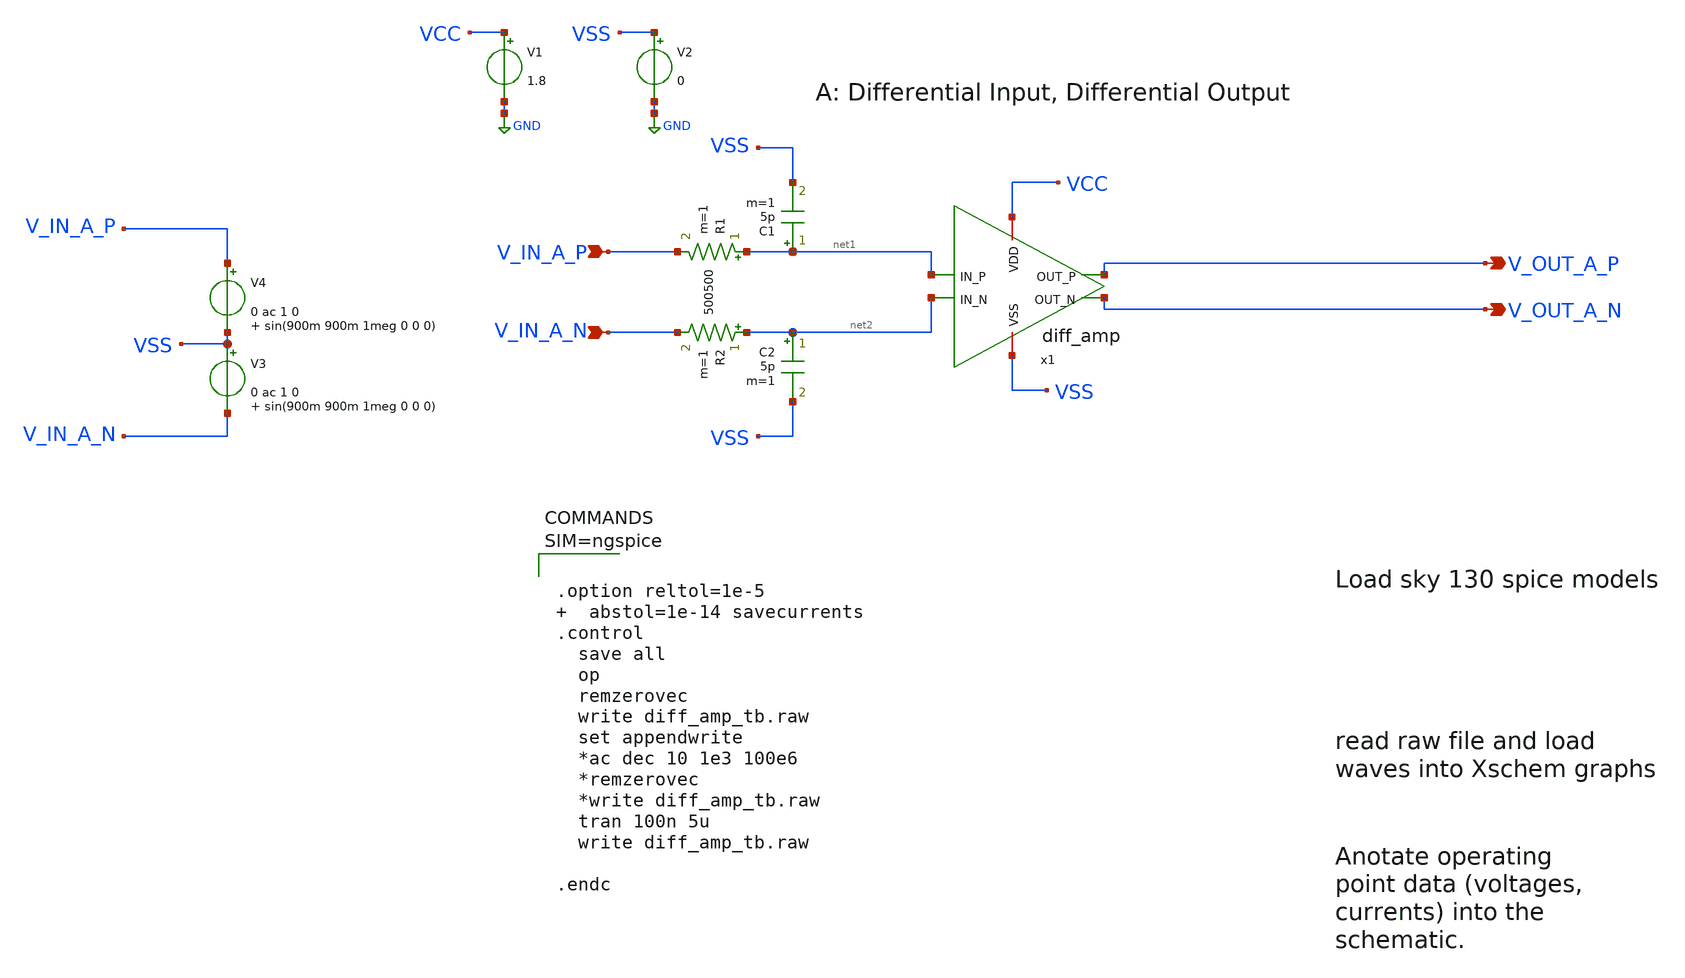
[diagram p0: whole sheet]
** sch_path: xschem/diff_amp_tb.sch
**.subckt diff_amp_tb V_IN_A_P V_OUT_A_N V_OUT_A_P V_IN_A_N
*.ipin V_IN_A_P
*.opin V_OUT_A_N
*.opin V_OUT_A_P
*.ipin V_IN_A_N
x1 VCC VSS net2 V_OUT_A_P V_OUT_A_N net1 diff_amp
V1 VCC GND 1.8
V2 VSS GND 0
V4 V_IN_A_P VSS 0 ac 1 0 sin(900m 900m 1meg 0 0 0)
R1 net1 V_IN_A_P 500 m=1
C1 net1 VSS 5p m=1
R2 net2 V_IN_A_N 500 m=1
C2 net2 VSS 5p m=1
V3 VSS V_IN_A_N 0 ac 1 0 sin(900m 900m 1meg 0 0 0)
**** begin user architecture code

** opencircuitdesign pdks install
.lib $::SKYWATER_MODELS/sky130.lib.spice tt





.option reltol=1e-5   abstol=1e-14 savecurrents
.control
  save all
  op
  remzerovec
  write diff_amp_tb.raw
  set appendwrite
  *ac dec 10 1e3 100e6
  *remzerovec
  *write diff_amp_tb.raw
  tran 100n 5u
  write diff_amp_tb.raw

.endc



**** end user architecture code
**.ends

* expanding   symbol:  diff_amp.sym # of pins=6
** sym_path: xschem/diff_amp.sym
** sch_path: xschem/diff_amp.sch
.subckt diff_amp VDD VSS IN_N OUT_P OUT_N IN_P
*.iopin VDD
*.iopin VSS
*.ipin IN_N
*.ipin IN_P
*.opin OUT_P
*.opin OUT_N
XM6 net1 net1 VSS VSS sky130_fd_pr__nfet_01v8 L=0.38 W=3.6 nf=2 ad='int((nf+1)/2) * W/nf * 0.29' as='int((nf+2)/2) * W/nf * 0.29'
+ pd='2*int((nf+1)/2) * (W/nf + 0.29)' ps='2*int((nf+2)/2) * (W/nf + 0.29)' nrd='0.29 / W' nrs='0.29 / W'
+ sa=0 sb=0 sd=0 mult=1 m=1
XM4 OUT_P OUT_P VDD VDD sky130_fd_pr__pfet_01v8_lvt L=0.38 W=3.6 nf=2 ad='int((nf+1)/2) * W/nf * 0.29'
+ as='int((nf+2)/2) * W/nf * 0.29' pd='2*int((nf+1)/2) * (W/nf + 0.29)' ps='2*int((nf+2)/2) * (W/nf + 0.29)'
+ nrd='0.29 / W' nrs='0.29 / W' sa=0 sb=0 sd=0 mult=1 m=1
XR2 net1 VDD VSS sky130_fd_pr__res_xhigh_po_2p85 L=1.85 mult=10 m=10
XM3 VX net1 VSS VSS sky130_fd_pr__nfet_01v8 L=0.38 W=3.6 nf=2 ad='int((nf+1)/2) * W/nf * 0.29' as='int((nf+2)/2) * W/nf * 0.29'
+ pd='2*int((nf+1)/2) * (W/nf + 0.29)' ps='2*int((nf+2)/2) * (W/nf + 0.29)' nrd='0.29 / W' nrs='0.29 / W'
+ sa=0 sb=0 sd=0 mult=1 m=1
XM1 OUT_P IN_P VX VSS sky130_fd_pr__nfet_01v8 L=0.38 W=3.6 nf=2 ad='int((nf+1)/2) * W/nf * 0.29' as='int((nf+2)/2) * W/nf * 0.29'
+ pd='2*int((nf+1)/2) * (W/nf + 0.29)' ps='2*int((nf+2)/2) * (W/nf + 0.29)' nrd='0.29 / W' nrs='0.29 / W'
+ sa=0 sb=0 sd=0 mult=1 m=1
XM2 OUT_N IN_N VX VSS sky130_fd_pr__nfet_01v8 L=0.38 W=3.6 nf=2 ad='int((nf+1)/2) * W/nf * 0.29' as='int((nf+2)/2) * W/nf * 0.29'
+ pd='2*int((nf+1)/2) * (W/nf + 0.29)' ps='2*int((nf+2)/2) * (W/nf + 0.29)' nrd='0.29 / W' nrs='0.29 / W'
+ sa=0 sb=0 sd=0 mult=1 m=1
XM5 OUT_N OUT_P VDD VDD sky130_fd_pr__pfet_01v8_lvt L=0.38 W=3.6 nf=2 ad='int((nf+1)/2) * W/nf * 0.29'
+ as='int((nf+2)/2) * W/nf * 0.29' pd='2*int((nf+1)/2) * (W/nf + 0.29)' ps='2*int((nf+2)/2) * (W/nf + 0.29)'
+ nrd='0.29 / W' nrs='0.29 / W' sa=0 sb=0 sd=0 mult=1 m=1
.ends

.GLOBAL GND
.end
